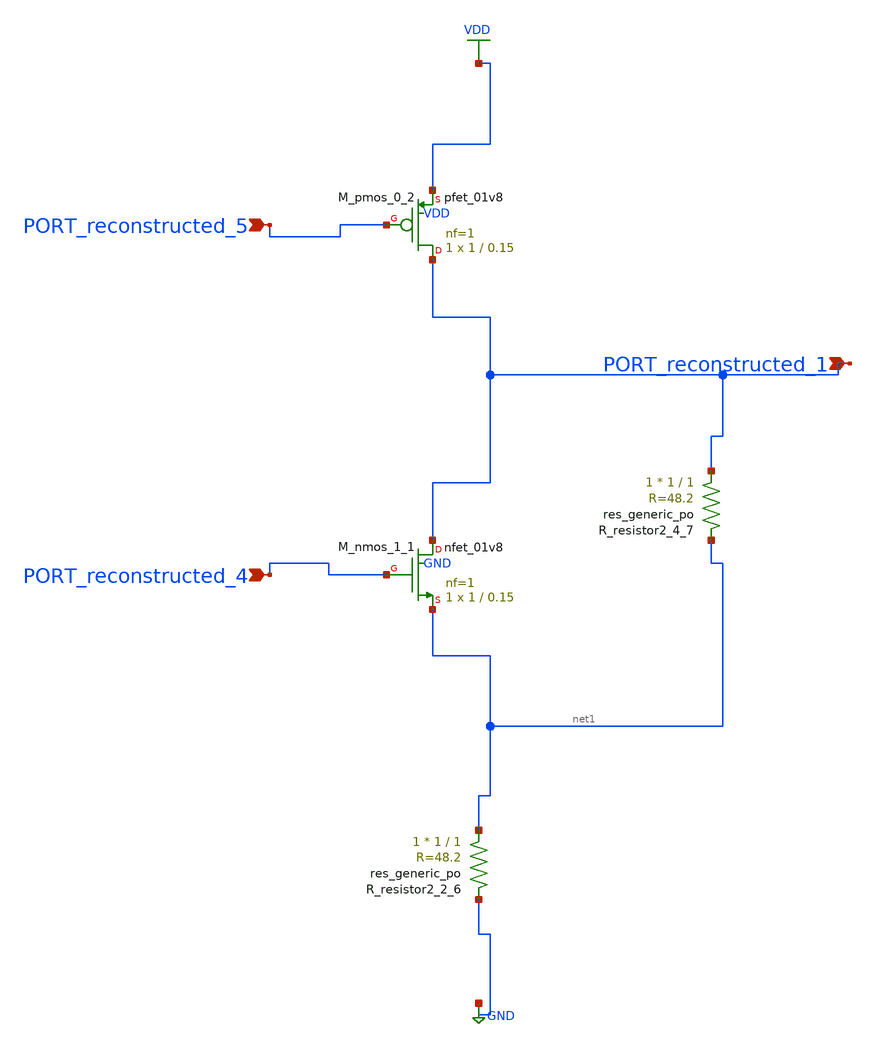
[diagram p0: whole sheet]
** sch_path: schematics/AMSNet/512.sch
**.subckt 512 PORT_reconstructed_5 PORT_reconstructed_1 PORT_reconstructed_4
*.ipin PORT_reconstructed_5
*.ipin PORT_reconstructed_1
*.ipin PORT_reconstructed_4
XM_nmos_1_1 PORT_reconstructed_1 PORT_reconstructed_4 net1 GND sky130_fd_pr__nfet_01v8 L=0.15 W=1 nf=1
+ ad='int((1 + 1)/2) * 1 / 1 * 0.29' as='int((1 + 2)/2) * 1 / 1 * 0.29' pd='2*int((1 + 1)/2) * (1 / 1 + 0.29)'
+ ps='2*int((1 + 2)/2) * (1 / 1 + 0.29)' nrd='0.29 / 1 ' nrs='0.29 / 1 ' sa=0 sb=0 sd=0 mult=1 m=1
XM_pmos_0_2 PORT_reconstructed_1 PORT_reconstructed_5 VDD VDD sky130_fd_pr__pfet_01v8 L=0.15 W=1 nf=1
+ ad='int((1 + 1)/2) * 1 / 1 * 0.29' as='int((1 + 2)/2) * 1 / 1 * 0.29' pd='2*int((1 + 1)/2) * (1 / 1 + 0.29)'
+ ps='2*int((1 + 2)/2) * (1 / 1 + 0.29)' nrd='0.29 / 1 ' nrs='0.29 / 1 ' sa=0 sb=0 sd=0 mult=1 m=1
XR_resistor2_2_6 net1 GND sky130_fd_pr__res_generic_po W=1 L=1 m=1
XR_resistor2_4_7 PORT_reconstructed_1 net1 sky130_fd_pr__res_generic_po W=1 L=1 m=1
**.ends
.GLOBAL GND
.GLOBAL VDD
.end
